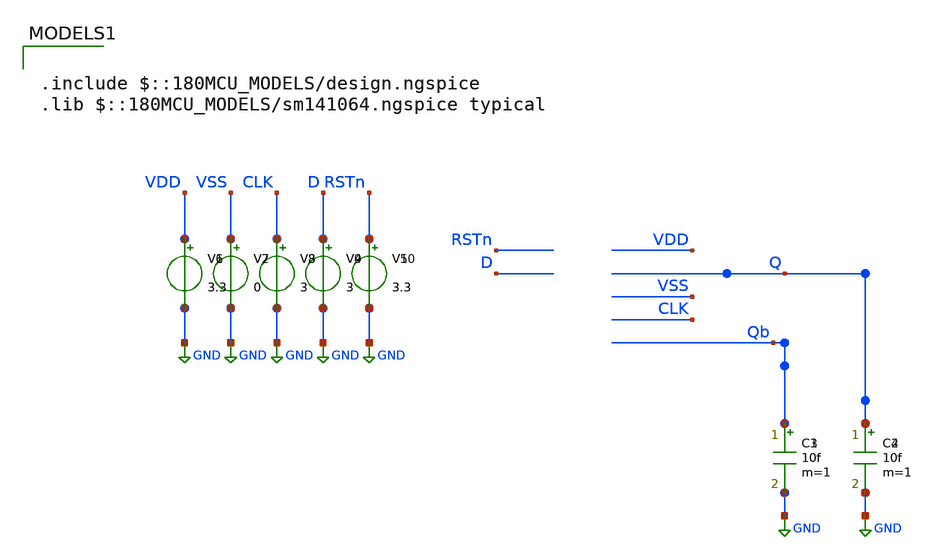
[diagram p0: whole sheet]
** sch_path: CAD6/DFF_Ray/DFF_Loop_PostPex_Testbench.sch
**.subckt DFF_Loop_PostPex_Testbench
V1 VDD GND 3.3
V2 VSS GND 0
V3 CLK GND 3
V4 D GND 3
V5 RSTn GND 3.3
C1 Qb GND 10f m=1
C2 Q GND 10f m=1
V6 VDD GND 3.3
V7 VSS GND 0
V8 CLK GND 3
V9 D GND 3
V10 RSTn GND 3.3
C3 Qb GND 10f m=1
C4 Q GND 10f m=1
**** begin user architecture code

.include $::180MCU_MODELS/design.ngspice
.lib $::180MCU_MODELS/sm141064.ngspice typical




.subckt DFF_flat RSTn Q CLK D Qb VSS VDD
X0 a_1071_1500# a_n907_1431# VDD.t27 VDD.t26 pfet_03v3 ad=1.04p pd=4.52u as=2.6p ps=9.3u w=4u
+ l=0.28u
X1 a_3022_1567# a_2285_219# VDD.t1 VDD.t0 pfet_03v3 ad=0.52p pd=2.52u as=1.3p ps=5.3u w=2u l=0.28u
X2 a_n907_1431# a_n2195_1438.t2 VSS.t10 VSS.t9 nfet_03v3 ad=0.61p pd=3.22u as=0.61p ps=3.22u w=1u
+ l=0.28u
X3 Q.t0 a_6555_1638# VSS.t19 VSS.t18 nfet_03v3 ad=0.61p pd=3.22u as=0.61p ps=3.22u w=1u l=0.28u
X4 a_7454_2228# a_n2195_1438.t3 VSS.t8 VSS.t7 nfet_03v3 ad=0.52p pd=2.52u as=1.22p ps=5.22u w=2u
+ l=0.28u
X5 a_8183_2228# a_n907_1431# VDD.t25 VDD.t24 pfet_03v3 ad=1.04p pd=4.52u as=2.6p ps=9.3u w=4u
+ l=0.28u
X6 VDD.t15 RSTn.t0 a_3022_1567# VDD.t14 pfet_03v3 ad=1.3p pd=5.3u as=0.52p ps=2.52u w=2u l=0.28u
X7 a_2285_219# a_1231_771# VSS.t23 VSS.t22 nfet_03v3 ad=0.61p pd=3.22u as=0.61p ps=3.22u w=1u
+ l=0.28u
X8 VDD.t8 a_5268_1150# a_6555_1638# VDD.t7 pfet_03v3 ad=1.3p pd=5.3u as=0.52p ps=2.52u w=2u l=0.28u
X9 a_6555_912# RSTn.t1 VSS.t4 VSS.t3 nfet_03v3 ad=0.52p pd=2.52u as=1.22p ps=5.22u w=2u l=0.28u
X10 VSS.t1 RSTn.t2 a_3975_879# VSS.t0 nfet_03v3 ad=1.22p pd=5.22u as=0.52p ps=2.52u w=2u l=0.28u
X11 Qb.t0 a_9035_317# VSS.t13 VSS.t12 nfet_03v3 ad=0.61p pd=3.22u as=0.61p ps=3.22u w=1u l=0.28u
X12 a_3022_1567# a_n907_1431# a_1231_771# VSS.t25 nfet_03v3 ad=0.61p pd=3.22u as=0.61p ps=3.22u w=1u
+ l=0.28u
X13 a_9035_317# a_6555_1638# VSS.t17 VSS.t16 nfet_03v3 ad=0.61p pd=3.22u as=0.61p ps=3.22u w=1u
+ l=0.28u
X14 a_3975_879# a_2285_219# a_3022_1567# VSS.t2 nfet_03v3 ad=0.52p pd=2.52u as=1.22p ps=5.22u w=2u
+ l=0.28u
X15 a_n2195_1438.t1 CLK.t0 VSS.t21 VSS.t20 nfet_03v3 ad=0.61p pd=3.22u as=0.61p ps=3.22u w=1u
+ l=0.28u
X16 Q.t1 a_6555_1638# VDD.t13 VDD.t12 pfet_03v3 ad=1.3p pd=5.3u as=1.3p ps=5.3u w=2u l=0.28u
X17 a_1071_771# a_n2195_1438.t4 VSS.t6 VSS.t5 nfet_03v3 ad=0.52p pd=2.52u as=1.22p ps=5.22u w=2u
+ l=0.28u
X18 a_5268_1150# a_n907_1431# a_2285_219# VSS.t24 nfet_03v3 ad=0.61p pd=3.22u as=0.61p ps=3.22u w=1u
+ l=0.28u
X19 a_n907_1431# a_n2195_1438.t5 VDD.t22 VDD.t21 pfet_03v3 ad=1.3p pd=5.3u as=1.3p ps=5.3u w=2u
+ l=0.28u
X20 a_3022_1567# a_n2195_1438.t6 a_1231_771# VDD.t16 pfet_03v3 ad=1.3p pd=5.3u as=1.3p ps=5.3u w=2u
+ l=0.28u
X21 a_6555_1638# RSTn.t3 VDD.t4 VDD.t3 pfet_03v3 ad=0.52p pd=2.52u as=1.3p ps=5.3u w=2u l=0.28u
X22 a_5268_1150# a_n2195_1438.t7 a_2285_219# VDD.t2 pfet_03v3 ad=1.3p pd=5.3u as=1.3p ps=5.3u w=2u
+ l=0.28u
X23 a_2285_219# a_1231_771# VDD.t20 VDD.t19 pfet_03v3 ad=1.3p pd=5.3u as=1.3p ps=5.3u w=2u l=0.28u
X24 a_1231_771# D.t0 a_1071_771# VSS.t11 nfet_03v3 ad=1.22p pd=5.22u as=0.52p ps=2.52u w=2u l=0.28u
X25 a_n2195_1438.t0 CLK.t1 VDD.t18 VDD.t17 pfet_03v3 ad=1.3p pd=5.3u as=1.3p ps=5.3u w=2u l=0.28u
X26 Qb.t1 a_9035_317# VDD.t6 VDD.t5 pfet_03v3 ad=1.3p pd=5.3u as=1.3p ps=5.3u w=2u l=0.28u
X27 a_5268_1150# a_6555_1638# a_7454_2228# VSS.t15 nfet_03v3 ad=1.22p pd=5.22u as=0.52p ps=2.52u
+ w=2u l=0.28u
X28 a_6555_1638# a_5268_1150# a_6555_912# VSS.t14 nfet_03v3 ad=1.22p pd=5.22u as=0.52p ps=2.52u w=2u
+ l=0.28u
X29 a_9035_317# a_6555_1638# VDD.t11 VDD.t10 pfet_03v3 ad=1.3p pd=5.3u as=1.3p ps=5.3u w=2u l=0.28u
X30 a_5268_1150# a_6555_1638# a_8183_2228# VDD.t9 pfet_03v3 ad=2.6p pd=9.3u as=1.04p ps=4.52u w=4u
+ l=0.28u
X31 a_1231_771# D.t1 a_1071_1500# VDD.t23 pfet_03v3 ad=2.6p pd=9.3u as=1.04p ps=4.52u w=4u l=0.28u
R0 VDD.n11 VDD.t2 395.863
R1 VDD.n15 VDD.t16 395.464
R2 VDD.n17 VDD.t17 386.182
R3 VDD.n18 VDD.t21 386.182
R4 VDD.n2 VDD.t12 386.182
R5 VDD.n12 VDD.t14 386.026
R6 VDD.n8 VDD.t3 386.026
R7 VDD.n5 VDD.t5 385.858
R8 VDD.n3 VDD.t10 385.858
R9 VDD.n0 VDD.t19 385.858
R10 VDD.n20 VDD.t26 241.577
R11 VDD.n1 VDD.t24 241.577
R12 VDD.t14 VDD.t0 236.686
R13 VDD.t3 VDD.t7 236.686
R14 VDD.t26 VDD.t23 148.7
R15 VDD.t24 VDD.t9 148.7
R16 VDD.n16 VDD.n0 11.2146
R17 VDD.n21 VDD.n19 10.9694
R18 VDD.n10 VDD.n7 10.694
R19 VDD.n21 VDD.n20 9.9254
R20 VDD.n14 VDD.n13 9.9074
R21 VDD.n10 VDD.n9 9.62838
R22 VDD.n13 VDD.t1 4.20008
R23 VDD.n9 VDD.t8 4.16561
R24 VDD.n5 VDD.t6 3.52831
R25 VDD.n3 VDD.t11 3.52831
R26 VDD.n0 VDD.t20 3.52831
R27 VDD.n12 VDD.t15 3.20383
R28 VDD.n17 VDD.t18 3.20383
R29 VDD.n18 VDD.t22 3.20383
R30 VDD.n8 VDD.t4 3.20383
R31 VDD.n2 VDD.t13 3.20383
R32 VDD.n19 VDD.n17 2.19361
R33 VDD.n4 VDD.n2 1.66763
R34 VDD.n20 VDD.t27 1.61523
R35 VDD.n1 VDD.t25 1.61523
R36 VDD.n6 VDD.n5 1.24609
R37 VDD.n7 VDD.n6 0.626994
R38 VDD.n7 VDD.n1 0.597342
R39 VDD.n6 VDD.n4 0.5165
R40 VDD.n19 VDD.n18 0.483789
R41 VDD.n4 VDD.n3 0.430289
R42 VDD.n13 VDD.n12 0.372822
R43 VDD.n9 VDD.n8 0.367349
R44 VDD.n15 VDD.n14 0.345345
R45 VDD.n14 VDD.n11 0.299878
R46 VDD VDD.n16 0.232029
R47 VDD.n11 VDD.n10 0.212909
R48 VDD.n16 VDD.n15 0.173039
R49 VDD VDD.n21 0.0531943
R50 a_n2195_1438.n0 a_n2195_1438.t3 87.7196
R51 a_n2195_1438.n4 a_n2195_1438.t5 51.0281
R52 a_n2195_1438.n1 a_n2195_1438.t6 50.6747
R53 a_n2195_1438.n0 a_n2195_1438.t7 50.2216
R54 a_n2195_1438.n2 a_n2195_1438.t4 46.3543
R55 a_n2195_1438.n4 a_n2195_1438.t2 24.5076
R56 a_n2195_1438.n2 a_n2195_1438.n1 10.22
R57 a_n2195_1438.n3 a_n2195_1438.t1 9.16629
R58 a_n2195_1438.n5 a_n2195_1438.n4 9.1542
R59 a_n2195_1438.t0 a_n2195_1438.n5 4.15419
R60 a_n2195_1438.n3 a_n2195_1438.n2 2.78897
R61 a_n2195_1438.n1 a_n2195_1438.n0 2.00183
R62 a_n2195_1438.n5 a_n2195_1438.n3 0.161929
R63 VSS.n14 VSS.t12 226642
R64 VSS.n18 VSS.n14 184560
R65 VSS.n44 VSS.n43 133540
R66 VSS.n39 VSS.n2 17254.7
R67 VSS.t15 VSS.n11 14122.1
R68 VSS.n44 VSS.n39 11797.5
R69 VSS.t7 VSS.n29 9648.44
R70 VSS.n39 VSS.n3 8020.78
R71 VSS.n16 VSS.n15 7126.25
R72 VSS.n15 VSS.n11 6081.19
R73 VSS.n15 VSS.n12 5511.42
R74 VSS.n30 VSS.t15 5510.19
R75 VSS.n30 VSS.n8 5387.1
R76 VSS.n32 VSS.n31 5356.33
R77 VSS.n5 VSS.n2 4515.96
R78 VSS.n31 VSS.n3 4279.67
R79 VSS.n31 VSS.n30 3896.87
R80 VSS.n29 VSS.n26 3021.58
R81 VSS.n39 VSS.n38 2668.72
R82 VSS.n9 VSS.n3 2106.65
R83 VSS.t7 VSS.n12 1568.53
R84 VSS.n16 VSS.t18 1415.5
R85 VSS.n18 VSS.t16 1388.38
R86 VSS.n44 VSS.t9 1384.01
R87 VSS.n43 VSS.n41 1373.43
R88 VSS.n45 VSS.n44 1305.79
R89 VSS.n17 VSS.n16 1071.84
R90 VSS.n19 VSS.n18 1060.83
R91 VSS.n38 VSS.t22 1027.96
R92 VSS.t24 VSS.n32 881.659
R93 VSS.t22 VSS.n5 865.283
R94 VSS.t2 VSS.n9 798.481
R95 VSS.n26 VSS.t18 795.788
R96 VSS.n19 VSS.t12 789.602
R97 VSS.t16 VSS.n17 783.51
R98 VSS.n28 VSS.n8 700.11
R99 VSS.n33 VSS.n8 699.832
R100 VSS.n32 VSS.n10 699.032
R101 VSS.n9 VSS.t25 691.242
R102 VSS.n2 VSS.t11 568.894
R103 VSS.n29 VSS.t14 525.971
R104 VSS.t15 VSS.t7 489.642
R105 VSS.n45 VSS.t5 480.486
R106 VSS.n10 VSS.t0 452.394
R107 VSS.n14 VSS.n11 450.853
R108 VSS.n33 VSS.t24 446.183
R109 VSS.t3 VSS.n28 444.233
R110 VSS.t20 VSS.n42 388.132
R111 VSS.n41 VSS.t9 377.731
R112 VSS.n37 VSS.t25 363.048
R113 VSS.t11 VSS.t5 307.51
R114 VSS.t0 VSS.t2 289.533
R115 VSS.t14 VSS.t3 284.308
R116 VSS.n38 VSS.n37 275.916
R117 VSS.n43 VSS.t20 194.91
R118 VSS.n37 VSS.n36 21.3351
R119 VSS.n34 VSS.n33 20.975
R120 VSS.n23 VSS.n22 11.1066
R121 VSS.n26 VSS.n25 10.4858
R122 VSS.n41 VSS.n40 10.4005
R123 VSS.n5 VSS.n4 10.4005
R124 VSS.n20 VSS.n19 10.4005
R125 VSS.n17 VSS.n13 10.4005
R126 VSS.n42 VSS.n1 10.3684
R127 VSS.n35 VSS.n6 10.1004
R128 VSS.n47 VSS.n46 10.1003
R129 VSS.n27 VSS.n7 10.0608
R130 VSS.n40 VSS.n1 9.5066
R131 VSS.n25 VSS.n24 9.40565
R132 VSS.n24 VSS.n21 9.3605
R133 VSS.n4 VSS.n0 9.36007
R134 VSS.n40 VSS.t10 8.98866
R135 VSS.n42 VSS.t21 8.98866
R136 VSS.n4 VSS.t23 8.98866
R137 VSS.n13 VSS.t17 8.94247
R138 VSS.n20 VSS.t13 8.94247
R139 VSS.n25 VSS.t19 8.90339
R140 VSS.n46 VSS.t6 3.5074
R141 VSS.n22 VSS.t8 3.5074
R142 VSS.n6 VSS.t1 3.5041
R143 VSS.n27 VSS.t4 3.5041
R144 VSS.n46 VSS.n45 3.46717
R145 VSS.n10 VSS.n6 3.46717
R146 VSS.n22 VSS.n12 3.46717
R147 VSS.n28 VSS.n27 3.46717
R148 VSS.n47 VSS.n1 2.24722
R149 VSS.n21 VSS.n20 1.29511
R150 VSS.n36 VSS.n35 0.414593
R151 VSS VSS.n0 0.279127
R152 VSS.n23 VSS.n7 0.240655
R153 VSS.n21 VSS.n13 0.238942
R154 VSS.n35 VSS.n34 0.225966
R155 VSS.n36 VSS.n0 0.173272
R156 VSS.n24 VSS.n23 0.151122
R157 VSS.n34 VSS.n7 0.146459
R158 VSS VSS.n47 0.00399741
R159 Q Q.t0 9.28486
R160 Q Q.t1 4.29561
R161 RSTn.n1 RSTn.t0 50.7239
R162 RSTn.n0 RSTn.t1 50.7239
R163 RSTn.n1 RSTn.t2 37.5434
R164 RSTn.n0 RSTn.t3 37.5434
R165 RSTn RSTn.n0 12.0066
R166 RSTn RSTn.n1 8.00751
R167 Qb Qb.t0 9.32629
R168 Qb Qb.t1 4.25419
R169 CLK.n0 CLK.t1 51.0281
R170 CLK.n0 CLK.t0 24.5076
R171 CLK CLK.n0 8.47482
R172 D.n0 D.t1 77.0995
R173 D.n0 D.t0 37.5434
R174 D D.n0 8.00642
C0 D VDD 0.13303f
C1 Q VDD 0.27479f
C2 a_6555_1638# a_n907_1431# 0.31084f
C3 a_5268_1150# RSTn 0.26779f
C4 VDD a_8183_2228# 0.31677f
C5 a_1231_771# a_3022_1567# 0.24466f
C6 a_5268_1150# a_2285_219# 0.24106f
C7 RSTn a_2285_219# 0.26464f
C8 a_6555_1638# a_6555_912# 0.13246f
C9 VDD a_3022_1567# 0.70996f
C10 a_3975_879# a_3022_1567# 0.13226f
C11 VDD a_6555_1638# 1.43768f
C12 a_1071_1500# a_1231_771# 0.28032f
C13 Q a_6555_1638# 0.2423f
C14 a_9035_317# VDD 0.53205f
C15 a_1071_1500# VDD 0.29881f
C16 a_2285_219# a_n907_1431# 0.35134f
C17 CLK VDD 0.25038f
C18 a_1231_771# a_1071_771# 0.11961f
C19 a_5268_1150# VDD 0.88681f
C20 RSTn VDD 1.22466f
C21 m1_2226_1141# a_2285_219# 0.13517f
C22 Qb VDD 0.1711f
C23 VDD a_2285_219# 0.3928f
C24 a_1231_771# a_n907_1431# 0.20468f
C25 a_5268_1150# a_8183_2228# 0.28027f
C26 VDD a_n907_1431# 1.52577f
C27 a_5268_1150# a_6555_1638# 0.23736f
C28 VDD a_1231_771# 0.89549f
C29 Q a_n907_1431# 0.12174f
C30 a_2285_219# a_3022_1567# 0.20168f
C31 a_5268_1150# a_7454_2228# 0.12027f
C32 Qb VSS 0.42789f
C33 Q VSS 0.25938f
C34 RSTn VSS 1.85481f
C35 D VSS 0.26137f
C36 CLK VSS 0.50463f
C37 VDD VSS 28.63657f
C38 a_9035_317# VSS 0.89696f
C39 a_6555_912# VSS 0.13827f
C40 a_3975_879# VSS 0.13382f
C41 a_1071_771# VSS 0.13922f
C42 a_7454_2228# VSS 0.12773f
C43 a_6555_1638# VSS 3.50714f
C44 a_2285_219# VSS 2.34894f
C45 a_3022_1567# VSS 0.73695f
C46 a_n907_1431# VSS 5.87311f
C47 a_1231_771# VSS 1.78471f
C48 a_5268_1150# VSS 2.50453f
C49 a_n2195_1438.n0 VSS 0.57441f
C50 a_n2195_1438.n1 VSS 0.61259f
C51 a_n2195_1438.n2 VSS 0.45497f
C52 a_n2195_1438.n3 VSS 0.20435f
C53 a_n2195_1438.n5 VSS 0.20515f
C54 VDD.n10 VSS 0.28207f
C55 VDD.n11 VSS 0.13236f
C56 VDD.n14 VSS 0.10725f
C57 VDD.n15 VSS 0.12595f
.ends


X0 RSTn Q CLK D Qb VSS VDD DFF_flat





.control
save all

** Define input signals
let fclock = 10e6
let clockper = 1/fclock
let inputper = clockper*2
let resetper = clockper*8
let clocktfr = 0.01*clockper
let clockton = 0.5*clockper - 2*clocktfr
let resettfr = 0.01*resetper
let reseton = 0.5*resetper - 2*resettfr
let inputtfr = 0.01*inputper
let inputton = 0.5*inputper - 2*inputtfr

** Define transient params
let tstop = 10*clockper
let tstep = 0.001*clockper

** Set source
alter @v3[DC] = 0.0
alter @v3[PULSE] = [ 0 3.3 150n  $&clocktfr $&clocktfr $&clockton $&clockper 0 ]
alter @v4[PULSE] = [ 0 3.3 0 $&inputtfr $&inputtfr $&inputton $&inputper 0]
alter @v5[PULSE] = [ 3.3 0 0 $&resettfr $&resettfr $&reseton $&resetper 0]

**Set sweep parameters
let setuptimestart = 200p
let setuptimeend = 0p
let deltatime = 100p
let setuptime = setuptimestart

** Sweep Simulations
while setuptime ge setuptimeend
    reset
    alter @v3[PULSE] = [ 0 3.3 $&(200n-setuptime)  $&clocktfr $&clocktfr $&clockton $&clockper 0 ]
    tran $&tstep $&tstop
    setplot tran1
    meas tran TRIG v(clk) VAL=0.1 RISE=6 TARG v(q) VAL=0.1 FALL=2
    let setuptime = setuptime - deltatime
end

** Save waveform
write DFF_Post_Pex_Testbench.raw
.endc



.include $::180MCU_MODELS/design.ngspice
.lib $::180MCU_MODELS/sm141064.ngspice typical




.subckt DFF_flat RSTn Q CLK D Qb VSS VDD
X0 a_1071_1500# a_n907_1431# VDD.t27 VDD.t26 pfet_03v3 ad=1.04p pd=4.52u as=2.6p ps=9.3u w=4u
+ l=0.28u
X1 a_3022_1567# a_2285_219# VDD.t1 VDD.t0 pfet_03v3 ad=0.52p pd=2.52u as=1.3p ps=5.3u w=2u l=0.28u
X2 a_n907_1431# a_n2195_1438.t2 VSS.t10 VSS.t9 nfet_03v3 ad=0.61p pd=3.22u as=0.61p ps=3.22u w=1u
+ l=0.28u
X3 Q.t0 a_6555_1638# VSS.t19 VSS.t18 nfet_03v3 ad=0.61p pd=3.22u as=0.61p ps=3.22u w=1u l=0.28u
X4 a_7454_2228# a_n2195_1438.t3 VSS.t8 VSS.t7 nfet_03v3 ad=0.52p pd=2.52u as=1.22p ps=5.22u w=2u
+ l=0.28u
X5 a_8183_2228# a_n907_1431# VDD.t25 VDD.t24 pfet_03v3 ad=1.04p pd=4.52u as=2.6p ps=9.3u w=4u
+ l=0.28u
X6 VDD.t15 RSTn.t0 a_3022_1567# VDD.t14 pfet_03v3 ad=1.3p pd=5.3u as=0.52p ps=2.52u w=2u l=0.28u
X7 a_2285_219# a_1231_771# VSS.t23 VSS.t22 nfet_03v3 ad=0.61p pd=3.22u as=0.61p ps=3.22u w=1u
+ l=0.28u
X8 VDD.t8 a_5268_1150# a_6555_1638# VDD.t7 pfet_03v3 ad=1.3p pd=5.3u as=0.52p ps=2.52u w=2u l=0.28u
X9 a_6555_912# RSTn.t1 VSS.t4 VSS.t3 nfet_03v3 ad=0.52p pd=2.52u as=1.22p ps=5.22u w=2u l=0.28u
X10 VSS.t1 RSTn.t2 a_3975_879# VSS.t0 nfet_03v3 ad=1.22p pd=5.22u as=0.52p ps=2.52u w=2u l=0.28u
X11 Qb.t0 a_9035_317# VSS.t13 VSS.t12 nfet_03v3 ad=0.61p pd=3.22u as=0.61p ps=3.22u w=1u l=0.28u
X12 a_3022_1567# a_n907_1431# a_1231_771# VSS.t25 nfet_03v3 ad=0.61p pd=3.22u as=0.61p ps=3.22u w=1u
+ l=0.28u
X13 a_9035_317# a_6555_1638# VSS.t17 VSS.t16 nfet_03v3 ad=0.61p pd=3.22u as=0.61p ps=3.22u w=1u
+ l=0.28u
X14 a_3975_879# a_2285_219# a_3022_1567# VSS.t2 nfet_03v3 ad=0.52p pd=2.52u as=1.22p ps=5.22u w=2u
+ l=0.28u
X15 a_n2195_1438.t1 CLK.t0 VSS.t21 VSS.t20 nfet_03v3 ad=0.61p pd=3.22u as=0.61p ps=3.22u w=1u
+ l=0.28u
X16 Q.t1 a_6555_1638# VDD.t13 VDD.t12 pfet_03v3 ad=1.3p pd=5.3u as=1.3p ps=5.3u w=2u l=0.28u
X17 a_1071_771# a_n2195_1438.t4 VSS.t6 VSS.t5 nfet_03v3 ad=0.52p pd=2.52u as=1.22p ps=5.22u w=2u
+ l=0.28u
X18 a_5268_1150# a_n907_1431# a_2285_219# VSS.t24 nfet_03v3 ad=0.61p pd=3.22u as=0.61p ps=3.22u w=1u
+ l=0.28u
X19 a_n907_1431# a_n2195_1438.t5 VDD.t22 VDD.t21 pfet_03v3 ad=1.3p pd=5.3u as=1.3p ps=5.3u w=2u
+ l=0.28u
X20 a_3022_1567# a_n2195_1438.t6 a_1231_771# VDD.t16 pfet_03v3 ad=1.3p pd=5.3u as=1.3p ps=5.3u w=2u
+ l=0.28u
X21 a_6555_1638# RSTn.t3 VDD.t4 VDD.t3 pfet_03v3 ad=0.52p pd=2.52u as=1.3p ps=5.3u w=2u l=0.28u
X22 a_5268_1150# a_n2195_1438.t7 a_2285_219# VDD.t2 pfet_03v3 ad=1.3p pd=5.3u as=1.3p ps=5.3u w=2u
+ l=0.28u
X23 a_2285_219# a_1231_771# VDD.t20 VDD.t19 pfet_03v3 ad=1.3p pd=5.3u as=1.3p ps=5.3u w=2u l=0.28u
X24 a_1231_771# D.t0 a_1071_771# VSS.t11 nfet_03v3 ad=1.22p pd=5.22u as=0.52p ps=2.52u w=2u l=0.28u
X25 a_n2195_1438.t0 CLK.t1 VDD.t18 VDD.t17 pfet_03v3 ad=1.3p pd=5.3u as=1.3p ps=5.3u w=2u l=0.28u
X26 Qb.t1 a_9035_317# VDD.t6 VDD.t5 pfet_03v3 ad=1.3p pd=5.3u as=1.3p ps=5.3u w=2u l=0.28u
X27 a_5268_1150# a_6555_1638# a_7454_2228# VSS.t15 nfet_03v3 ad=1.22p pd=5.22u as=0.52p ps=2.52u
+ w=2u l=0.28u
X28 a_6555_1638# a_5268_1150# a_6555_912# VSS.t14 nfet_03v3 ad=1.22p pd=5.22u as=0.52p ps=2.52u w=2u
+ l=0.28u
X29 a_9035_317# a_6555_1638# VDD.t11 VDD.t10 pfet_03v3 ad=1.3p pd=5.3u as=1.3p ps=5.3u w=2u l=0.28u
X30 a_5268_1150# a_6555_1638# a_8183_2228# VDD.t9 pfet_03v3 ad=2.6p pd=9.3u as=1.04p ps=4.52u w=4u
+ l=0.28u
X31 a_1231_771# D.t1 a_1071_1500# VDD.t23 pfet_03v3 ad=2.6p pd=9.3u as=1.04p ps=4.52u w=4u l=0.28u
R0 VDD.n11 VDD.t2 395.863
R1 VDD.n15 VDD.t16 395.464
R2 VDD.n17 VDD.t17 386.182
R3 VDD.n18 VDD.t21 386.182
R4 VDD.n2 VDD.t12 386.182
R5 VDD.n12 VDD.t14 386.026
R6 VDD.n8 VDD.t3 386.026
R7 VDD.n5 VDD.t5 385.858
R8 VDD.n3 VDD.t10 385.858
R9 VDD.n0 VDD.t19 385.858
R10 VDD.n20 VDD.t26 241.577
R11 VDD.n1 VDD.t24 241.577
R12 VDD.t14 VDD.t0 236.686
R13 VDD.t3 VDD.t7 236.686
R14 VDD.t26 VDD.t23 148.7
R15 VDD.t24 VDD.t9 148.7
R16 VDD.n16 VDD.n0 11.2146
R17 VDD.n21 VDD.n19 10.9694
R18 VDD.n10 VDD.n7 10.694
R19 VDD.n21 VDD.n20 9.9254
R20 VDD.n14 VDD.n13 9.9074
R21 VDD.n10 VDD.n9 9.62838
R22 VDD.n13 VDD.t1 4.20008
R23 VDD.n9 VDD.t8 4.16561
R24 VDD.n5 VDD.t6 3.52831
R25 VDD.n3 VDD.t11 3.52831
R26 VDD.n0 VDD.t20 3.52831
R27 VDD.n12 VDD.t15 3.20383
R28 VDD.n17 VDD.t18 3.20383
R29 VDD.n18 VDD.t22 3.20383
R30 VDD.n8 VDD.t4 3.20383
R31 VDD.n2 VDD.t13 3.20383
R32 VDD.n19 VDD.n17 2.19361
R33 VDD.n4 VDD.n2 1.66763
R34 VDD.n20 VDD.t27 1.61523
R35 VDD.n1 VDD.t25 1.61523
R36 VDD.n6 VDD.n5 1.24609
R37 VDD.n7 VDD.n6 0.626994
R38 VDD.n7 VDD.n1 0.597342
R39 VDD.n6 VDD.n4 0.5165
R40 VDD.n19 VDD.n18 0.483789
R41 VDD.n4 VDD.n3 0.430289
R42 VDD.n13 VDD.n12 0.372822
R43 VDD.n9 VDD.n8 0.367349
R44 VDD.n15 VDD.n14 0.345345
R45 VDD.n14 VDD.n11 0.299878
R46 VDD VDD.n16 0.232029
R47 VDD.n11 VDD.n10 0.212909
R48 VDD.n16 VDD.n15 0.173039
R49 VDD VDD.n21 0.0531943
R50 a_n2195_1438.n0 a_n2195_1438.t3 87.7196
R51 a_n2195_1438.n4 a_n2195_1438.t5 51.0281
R52 a_n2195_1438.n1 a_n2195_1438.t6 50.6747
R53 a_n2195_1438.n0 a_n2195_1438.t7 50.2216
R54 a_n2195_1438.n2 a_n2195_1438.t4 46.3543
R55 a_n2195_1438.n4 a_n2195_1438.t2 24.5076
R56 a_n2195_1438.n2 a_n2195_1438.n1 10.22
R57 a_n2195_1438.n3 a_n2195_1438.t1 9.16629
R58 a_n2195_1438.n5 a_n2195_1438.n4 9.1542
R59 a_n2195_1438.t0 a_n2195_1438.n5 4.15419
R60 a_n2195_1438.n3 a_n2195_1438.n2 2.78897
R61 a_n2195_1438.n1 a_n2195_1438.n0 2.00183
R62 a_n2195_1438.n5 a_n2195_1438.n3 0.161929
R63 VSS.n14 VSS.t12 226642
R64 VSS.n18 VSS.n14 184560
R65 VSS.n44 VSS.n43 133540
R66 VSS.n39 VSS.n2 17254.7
R67 VSS.t15 VSS.n11 14122.1
R68 VSS.n44 VSS.n39 11797.5
R69 VSS.t7 VSS.n29 9648.44
R70 VSS.n39 VSS.n3 8020.78
R71 VSS.n16 VSS.n15 7126.25
R72 VSS.n15 VSS.n11 6081.19
R73 VSS.n15 VSS.n12 5511.42
R74 VSS.n30 VSS.t15 5510.19
R75 VSS.n30 VSS.n8 5387.1
R76 VSS.n32 VSS.n31 5356.33
R77 VSS.n5 VSS.n2 4515.96
R78 VSS.n31 VSS.n3 4279.67
R79 VSS.n31 VSS.n30 3896.87
R80 VSS.n29 VSS.n26 3021.58
R81 VSS.n39 VSS.n38 2668.72
R82 VSS.n9 VSS.n3 2106.65
R83 VSS.t7 VSS.n12 1568.53
R84 VSS.n16 VSS.t18 1415.5
R85 VSS.n18 VSS.t16 1388.38
R86 VSS.n44 VSS.t9 1384.01
R87 VSS.n43 VSS.n41 1373.43
R88 VSS.n45 VSS.n44 1305.79
R89 VSS.n17 VSS.n16 1071.84
R90 VSS.n19 VSS.n18 1060.83
R91 VSS.n38 VSS.t22 1027.96
R92 VSS.t24 VSS.n32 881.659
R93 VSS.t22 VSS.n5 865.283
R94 VSS.t2 VSS.n9 798.481
R95 VSS.n26 VSS.t18 795.788
R96 VSS.n19 VSS.t12 789.602
R97 VSS.t16 VSS.n17 783.51
R98 VSS.n28 VSS.n8 700.11
R99 VSS.n33 VSS.n8 699.832
R100 VSS.n32 VSS.n10 699.032
R101 VSS.n9 VSS.t25 691.242
R102 VSS.n2 VSS.t11 568.894
R103 VSS.n29 VSS.t14 525.971
R104 VSS.t15 VSS.t7 489.642
R105 VSS.n45 VSS.t5 480.486
R106 VSS.n10 VSS.t0 452.394
R107 VSS.n14 VSS.n11 450.853
R108 VSS.n33 VSS.t24 446.183
R109 VSS.t3 VSS.n28 444.233
R110 VSS.t20 VSS.n42 388.132
R111 VSS.n41 VSS.t9 377.731
R112 VSS.n37 VSS.t25 363.048
R113 VSS.t11 VSS.t5 307.51
R114 VSS.t0 VSS.t2 289.533
R115 VSS.t14 VSS.t3 284.308
R116 VSS.n38 VSS.n37 275.916
R117 VSS.n43 VSS.t20 194.91
R118 VSS.n37 VSS.n36 21.3351
R119 VSS.n34 VSS.n33 20.975
R120 VSS.n23 VSS.n22 11.1066
R121 VSS.n26 VSS.n25 10.4858
R122 VSS.n41 VSS.n40 10.4005
R123 VSS.n5 VSS.n4 10.4005
R124 VSS.n20 VSS.n19 10.4005
R125 VSS.n17 VSS.n13 10.4005
R126 VSS.n42 VSS.n1 10.3684
R127 VSS.n35 VSS.n6 10.1004
R128 VSS.n47 VSS.n46 10.1003
R129 VSS.n27 VSS.n7 10.0608
R130 VSS.n40 VSS.n1 9.5066
R131 VSS.n25 VSS.n24 9.40565
R132 VSS.n24 VSS.n21 9.3605
R133 VSS.n4 VSS.n0 9.36007
R134 VSS.n40 VSS.t10 8.98866
R135 VSS.n42 VSS.t21 8.98866
R136 VSS.n4 VSS.t23 8.98866
R137 VSS.n13 VSS.t17 8.94247
R138 VSS.n20 VSS.t13 8.94247
R139 VSS.n25 VSS.t19 8.90339
R140 VSS.n46 VSS.t6 3.5074
R141 VSS.n22 VSS.t8 3.5074
R142 VSS.n6 VSS.t1 3.5041
R143 VSS.n27 VSS.t4 3.5041
R144 VSS.n46 VSS.n45 3.46717
R145 VSS.n10 VSS.n6 3.46717
R146 VSS.n22 VSS.n12 3.46717
R147 VSS.n28 VSS.n27 3.46717
R148 VSS.n47 VSS.n1 2.24722
R149 VSS.n21 VSS.n20 1.29511
R150 VSS.n36 VSS.n35 0.414593
R151 VSS VSS.n0 0.279127
R152 VSS.n23 VSS.n7 0.240655
R153 VSS.n21 VSS.n13 0.238942
R154 VSS.n35 VSS.n34 0.225966
R155 VSS.n36 VSS.n0 0.173272
R156 VSS.n24 VSS.n23 0.151122
R157 VSS.n34 VSS.n7 0.146459
R158 VSS VSS.n47 0.00399741
R159 Q Q.t0 9.28486
R160 Q Q.t1 4.29561
R161 RSTn.n1 RSTn.t0 50.7239
R162 RSTn.n0 RSTn.t1 50.7239
R163 RSTn.n1 RSTn.t2 37.5434
R164 RSTn.n0 RSTn.t3 37.5434
R165 RSTn RSTn.n0 12.0066
R166 RSTn RSTn.n1 8.00751
R167 Qb Qb.t0 9.32629
R168 Qb Qb.t1 4.25419
R169 CLK.n0 CLK.t1 51.0281
R170 CLK.n0 CLK.t0 24.5076
R171 CLK CLK.n0 8.47482
R172 D.n0 D.t1 77.0995
R173 D.n0 D.t0 37.5434
R174 D D.n0 8.00642
C0 D VDD 0.13303f
C1 Q VDD 0.27479f
C2 a_6555_1638# a_n907_1431# 0.31084f
C3 a_5268_1150# RSTn 0.26779f
C4 VDD a_8183_2228# 0.31677f
C5 a_1231_771# a_3022_1567# 0.24466f
C6 a_5268_1150# a_2285_219# 0.24106f
C7 RSTn a_2285_219# 0.26464f
C8 a_6555_1638# a_6555_912# 0.13246f
C9 VDD a_3022_1567# 0.70996f
C10 a_3975_879# a_3022_1567# 0.13226f
C11 VDD a_6555_1638# 1.43768f
C12 a_1071_1500# a_1231_771# 0.28032f
C13 Q a_6555_1638# 0.2423f
C14 a_9035_317# VDD 0.53205f
C15 a_1071_1500# VDD 0.29881f
C16 a_2285_219# a_n907_1431# 0.35134f
C17 CLK VDD 0.25038f
C18 a_1231_771# a_1071_771# 0.11961f
C19 a_5268_1150# VDD 0.88681f
C20 RSTn VDD 1.22466f
C21 m1_2226_1141# a_2285_219# 0.13517f
C22 Qb VDD 0.1711f
C23 VDD a_2285_219# 0.3928f
C24 a_1231_771# a_n907_1431# 0.20468f
C25 a_5268_1150# a_8183_2228# 0.28027f
C26 VDD a_n907_1431# 1.52577f
C27 a_5268_1150# a_6555_1638# 0.23736f
C28 VDD a_1231_771# 0.89549f
C29 Q a_n907_1431# 0.12174f
C30 a_2285_219# a_3022_1567# 0.20168f
C31 a_5268_1150# a_7454_2228# 0.12027f
C32 Qb VSS 0.42789f
C33 Q VSS 0.25938f
C34 RSTn VSS 1.85481f
C35 D VSS 0.26137f
C36 CLK VSS 0.50463f
C37 VDD VSS 28.63657f
C38 a_9035_317# VSS 0.89696f
C39 a_6555_912# VSS 0.13827f
C40 a_3975_879# VSS 0.13382f
C41 a_1071_771# VSS 0.13922f
C42 a_7454_2228# VSS 0.12773f
C43 a_6555_1638# VSS 3.50714f
C44 a_2285_219# VSS 2.34894f
C45 a_3022_1567# VSS 0.73695f
C46 a_n907_1431# VSS 5.87311f
C47 a_1231_771# VSS 1.78471f
C48 a_5268_1150# VSS 2.50453f
C49 a_n2195_1438.n0 VSS 0.57441f
C50 a_n2195_1438.n1 VSS 0.61259f
C51 a_n2195_1438.n2 VSS 0.45497f
C52 a_n2195_1438.n3 VSS 0.20435f
C53 a_n2195_1438.n5 VSS 0.20515f
C54 VDD.n10 VSS 0.28207f
C55 VDD.n11 VSS 0.13236f
C56 VDD.n14 VSS 0.10725f
C57 VDD.n15 VSS 0.12595f
.ends


X0 RSTn Q CLK D Qb VSS VDD DFF_flat





.control
save all

** Define input signals
let fclock = 10e6
let clockper = 1/fclock
let inputper = clockper*4
let resetper = clockper*8
let clocktfr = 0.01*clockper
let clockton = 0.5*clockper - 2*clocktfr
let resettfr = 0.01*resetper
let reseton = 0.5*resetper - 2*resettfr
let inputtfr = 0.01*inputper
let inputton = 0.5*inputper - 2*inputtfr

** Define transient params
let tstop = 10*clockper
let tstep = 0.001*clockper

** Set source
alter @v3[DC] = 0.0
alter @v3[PULSE] = [ 0 3.3 199.999n $&clocktfr $&clocktfr $&clockton $&clockper 0 ]
alter @v4[PULSE] = [ 0 3.3 0 $&inputtfr $&inputtfr $&inputton $&inputper 0]
**alter @v5[PULSE] = [ 3.3 0 0 $&resettfr $&resettfr $&reseton $&resetper 0]

** Simulations
op
dc v3 0 3.3 0.01
tran $&tstep $&tstop

** Save waveform
write DFF_Post_Pex_Testbench.raw
.endc


**** end user architecture code
**.ends
.GLOBAL GND
.end
